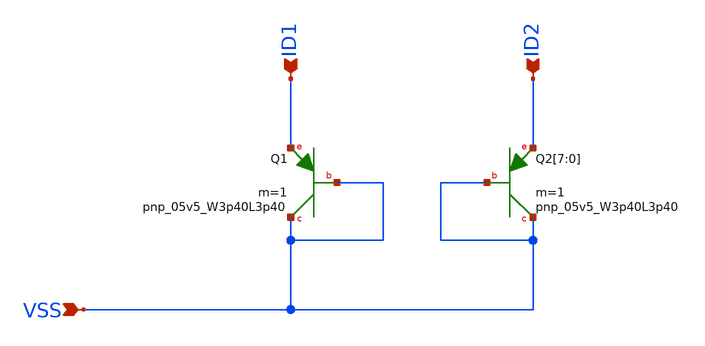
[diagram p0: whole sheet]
** sch_path: design/LELO_GR04_SKY130A/LELO_GR04_BG_BJT.sch
**.subckt LELO_GR04_BG_BJT VSS ID1 ID2
*.ipin VSS
*.ipin ID1
*.ipin ID2
XQ1 VSS VSS ID1 sky130_fd_pr__pnp_05v5_W3p40L3p40 m=1
XQ2[7] VSS VSS ID2 sky130_fd_pr__pnp_05v5_W3p40L3p40 m=1
XQ2[6] VSS VSS ID2 sky130_fd_pr__pnp_05v5_W3p40L3p40 m=1
XQ2[5] VSS VSS ID2 sky130_fd_pr__pnp_05v5_W3p40L3p40 m=1
XQ2[4] VSS VSS ID2 sky130_fd_pr__pnp_05v5_W3p40L3p40 m=1
XQ2[3] VSS VSS ID2 sky130_fd_pr__pnp_05v5_W3p40L3p40 m=1
XQ2[2] VSS VSS ID2 sky130_fd_pr__pnp_05v5_W3p40L3p40 m=1
XQ2[1] VSS VSS ID2 sky130_fd_pr__pnp_05v5_W3p40L3p40 m=1
XQ2[0] VSS VSS ID2 sky130_fd_pr__pnp_05v5_W3p40L3p40 m=1
**.ends
.end
